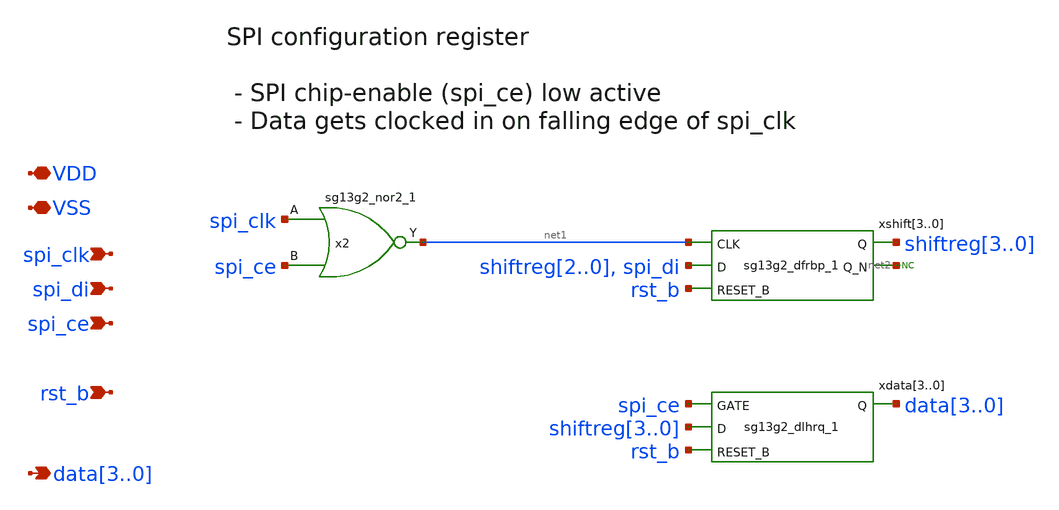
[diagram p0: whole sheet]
** sch_path: FLDO/design_data/xschem/spi_register.sch
* IHP-GmbH/IHP-Open-PDK/ihp-sg13g2/libs.tech/xschem/sg13g2_stdcells/sg13g2_nor2_1.sch:
* Copyright 2023 IHP PDK Authors
* Licensed under the Apache License, Version 2.0 (the "License");
**.subckt spi_register VDD spi_clk VSS data3,data2,data1,data0 spi_di spi_ce rst_b
*.iopin VDD
*.ipin spi_clk
*.iopin VSS
*.opin data3,data2,data1,data0
*.ipin spi_di
*.ipin spi_ce
*.ipin rst_b
xshift3 shiftreg3 net2[3] net1 shiftreg2 rst_b VDD VSS sg13g2_dfrbp_1
xshift2 shiftreg2 net2[2] net1 shiftreg1 rst_b VDD VSS sg13g2_dfrbp_1
xshift1 shiftreg1 net2[1] net1 shiftreg0 rst_b VDD VSS sg13g2_dfrbp_1
xshift0 shiftreg0 net2[0] net1 spi_di rst_b VDD VSS sg13g2_dfrbp_1
x2 net1 spi_clk spi_ce VDD VSS sg13g2_nor2_1
xdata3 shiftreg3 rst_b VGND VNB VPB VPWR data3 sg13g2_dlhrq_1
xdata2 shiftreg2 rst_b VGND VNB VPB VPWR data2 sg13g2_dlhrq_1
xdata1 shiftreg1 rst_b VGND VNB VPB VPWR data1 sg13g2_dlhrq_1
xdata0 shiftreg0 rst_b VGND VNB VPB VPWR data0 sg13g2_dlhrq_1
* noconn #net2
**.ends

* expanding   symbol:  sg13g2_stdcells/sg13g2_dfrbp_1.sym # of pins=5
** sym_path: sg13g2_stdcells/sg13g2_dfrbp_1.sym
** sch_path: sg13g2_stdcells/sg13g2_dfrbp_1.sch
.subckt sg13g2_dfrbp_1 Q Q_N CLK D RESET_B VDD VSS
*.ipin D
*.ipin RESET_B
*.ipin CLK
*.opin Q
*.opin Q_N
*.iopin VDD
*.iopin VSS
XM1 Db D net10 VSS sg13_lv_nmos w=420.00n l=130.00n ng=1 m=1 mm_ok=1
XM2 net10 RESET_B VSS VSS sg13_lv_nmos w=420.00n l=130.00n ng=1 m=1 mm_ok=1
XM3 net1 clkneg net9 VSS sg13_lv_nmos w=420.00n l=130.00n ng=1 m=1 mm_ok=1
XM4 net9 net1 VSS VSS sg13_lv_nmos w=420.00n l=130.00n ng=1 m=1 mm_ok=1
XM5 net1 net1 net5 VSS sg13_lv_nmos w=420.00n l=130.00n ng=1 m=1 mm_ok=1
XM6 net5 RESET_B VSS VSS sg13_lv_nmos w=420.00n l=130.00n ng=1 m=1 mm_ok=1
XM7 Q_N net1 VSS VSS sg13_lv_nmos w=740.00n l=130.00n ng=1 m=1 mm_ok=1
XM8 net2 net1 VSS VSS sg13_lv_nmos w=740.00n l=130.00n ng=1 m=1 mm_ok=1
XM9 Q net2 VSS VSS sg13_lv_nmos w=740.00n l=130.00n ng=1 m=1 mm_ok=1
XM10 clkneg CLK VSS VSS sg13_lv_nmos w=740.00n l=130.00n ng=1 m=1 mm_ok=1
XM11 clkpos clkneg VSS VSS sg13_lv_nmos w=740.00n l=130.00n ng=1 m=1 mm_ok=1
XM12 Db clkneg net3 VSS sg13_lv_nmos w=420.00n l=130.00n ng=1 m=1 mm_ok=1
XM13 net3 clkpos net8 VSS sg13_lv_nmos w=420.00n l=130.00n ng=1 m=1 mm_ok=1
XM14 net8 net3 net4 VSS sg13_lv_nmos w=420.00n l=130.00n ng=1 m=1 mm_ok=1
XM15 net4 RESET_B VSS VSS sg13_lv_nmos w=420.00n l=130.00n ng=1 m=1 mm_ok=1
XM16 net3 net3 VSS VSS sg13_lv_nmos w=740.00n l=130.00n ng=1 m=1 mm_ok=1
XM17 net3 clkpos net1 VSS sg13_lv_nmos w=740.00n l=130.00n ng=1 m=1 mm_ok=1
XM18 Db RESET_B VDD VDD sg13_lv_pmos w=420.00n l=130.00n ng=1 m=1 mm_ok=1
XM19 Db D VDD VDD sg13_lv_pmos w=420.00n l=130.00n ng=1 m=1 mm_ok=1
XM20 net7 net1 VDD VDD sg13_lv_pmos w=420.00n l=130.00n ng=1 m=1 mm_ok=1
XM21 net1 clkpos net7 VDD sg13_lv_pmos w=420.00n l=130.00n ng=1 m=1 mm_ok=1
XM22 net1 net1 VDD VDD sg13_lv_pmos w=420.00n l=130.00n ng=1 m=1 mm_ok=1
XM23 net1 RESET_B VDD VDD sg13_lv_pmos w=420.00n l=130.00n ng=1 m=1 mm_ok=1
XM24 Q_N net1 VDD VDD sg13_lv_pmos w=1.12u l=130.00n ng=1 m=1 mm_ok=1
XM25 net2 net1 VDD VDD sg13_lv_pmos w=1.12u l=130.00n ng=1 m=1 mm_ok=1
XM26 Q net2 VDD VDD sg13_lv_pmos w=1.12u l=130.00n ng=1 m=1 mm_ok=1
XM27 clkneg CLK VDD VDD sg13_lv_pmos w=1.12u l=130.00n ng=1 m=1 mm_ok=1
XM28 clkpos clkneg VDD VDD sg13_lv_pmos w=1.12u l=130.00n ng=1 m=1 mm_ok=1
XM29 Db clkpos net3 VDD sg13_lv_pmos w=420.00n l=130.00n ng=1 m=1 mm_ok=1
XM30 net6 net3 VDD VDD sg13_lv_pmos w=420.00n l=130.00n ng=1 m=1 mm_ok=1
XM31 net3 clkneg net6 VDD sg13_lv_pmos w=420.00n l=130.00n ng=1 m=1 mm_ok=1
XM32 net3 RESET_B VDD VDD sg13_lv_pmos w=420.00n l=130.00n ng=1 m=1 mm_ok=1
XM33 net3 net3 VDD VDD sg13_lv_pmos w=1.000u l=130.00n ng=1 m=1 mm_ok=1
XM34 net3 clkneg net1 VDD sg13_lv_pmos w=1.000u l=130.00n ng=1 m=1 mm_ok=1
.ends


* expanding   symbol:  sg13g2_stdcells/sg13g2_nor2_1.sym # of pins=3
** sym_path: sg13g2_stdcells/sg13g2_nor2_1.sym
** sch_path: sg13g2_stdcells/sg13g2_nor2_1.sch
.subckt sg13g2_nor2_1 Y A B VDD VSS
*.opin Y
*.ipin B
*.ipin A
*.iopin VDD
*.iopin VSS
XM1 Y A VSS VSS sg13_lv_nmos w=740.00n l=130.00n ng=1 m=1 mm_ok=1
XM2 Y B VSS VSS sg13_lv_nmos w=740.00n l=130.00n ng=1 m=1 mm_ok=1
XM3 net1 A VDD VDD sg13_lv_pmos w=1.12u l=130.00n ng=1 m=1 mm_ok=1
XM4 Y B net1 VDD sg13_lv_pmos w=1.12u l=130.00n ng=1 m=1 mm_ok=1
.ends

.end
